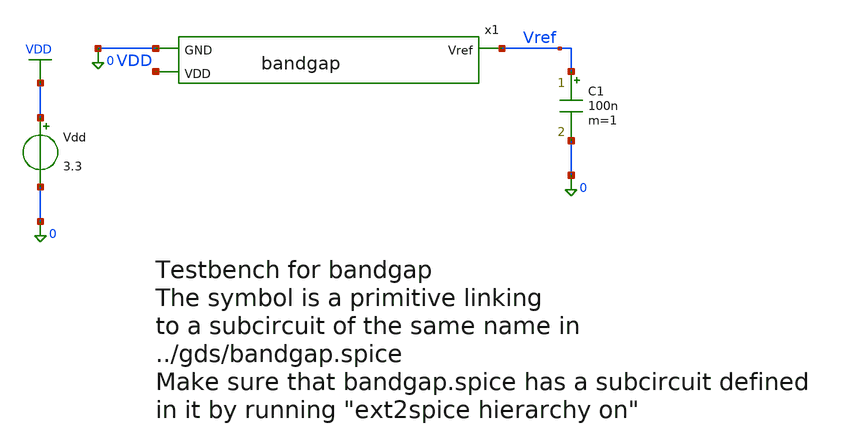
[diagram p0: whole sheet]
** sch_path: xschem/bandgap_tb.sch
* Copyright 2021 Stefan Frederik Schippers
* Licensed under the Apache License, Version 2.0 (the "License");
* you may not use this file except in compliance with the License.
* You may obtain a copy of the License at
* https://www.apache.org/licenses/LICENSE-2.0
* Unless required by applicable law or agreed to in writing, software
* distributed under the License is distributed on an "AS IS" BASIS,
* WITHOUT WARRANTIES OR CONDITIONS OF ANY KIND, either express or implied.
* See the License for the specific language governing permissions and
* limitations under the License.
**.subckt bandgap_tb
Vdd VDD 0 3.3
C1 Vref 0 100n m=1
x1 Vref VDD 0 bandgap
**** begin user architecture code

** opencircuitdesign pdks install
.lib $::SKYWATER_MODELS/sky130.lib.spice tt



.option wnflag=1
.include ../netlist/rcx/bandgap.spice
.save all
.control
set gnuplot_terminal=png/quit

op
#print x1.Vg1 x1.ve1 x1.vg10 x1.vg12 x1.vg2 x1.vg3 x1.vg5 x1.vs5
#tran 10n 10u
#plot V(Vref) title 'Vref vs time'

dc VDD 3.0 3.5 0.1
gnuplot bandgap_vref_vs_vdd V(Vref)  title 'Vref vs Vdd'  xlabel 'VDD' ylabel 'Vref'
#plot V(Vref) vs V(Vdd) title 'Vref vs Vdd'

dc VDD 3.0 3.5 0.02 TEMP -40 40 20
gnuplot bandgap_vref_vs_vdd_vs_temp V(Vref)  title 'Vref vs Vdd vs Temp (-40 to 40C)'  xlabel 'VDD' ylabel
+ 'Vref'
#plot V(Vref) Vs V(Vdd) title 'Vref vs Vdd vs Temp'

#dc TEMP -40 40 10
#plot V(Vref) title 'Vref vs Temp at VDD=3.3'

.endc


**** end user architecture code
**.ends

* expanding   symbol:  bandgap.sym # of pins=3
** sym_path: xschem/bandgap.sym
** sch_path: xschem/bandgap.sch
.subckt bandgap Vref VDD GND
*.opin Vref
*.ipin GND
*.ipin VDD
XM4 Vg3 Vg3 GND GND sky130_fd_pr__nfet_g5v0d10v5 L=1 W=20 nf=1 ad='int((1 + 1)/2) * 20 / 1 * 0.29' as='int((1 + 2)/2) * 20 / 1 * 0.29'
+ pd='2*int((1 + 1)/2) * (20 / 1 + 0.29)' ps='2*int((1 + 2)/2) * (20 / 1 + 0.29)' nrd='0.29 / 20 ' nrs='0.29 / 20 '
+ sa=0 sb=0 sd=0 mult=1 m=1
XQ1 GND GND Ve1 sky130_fd_pr__pnp_05v5_W3p40L3p40 m=24
XQ2 GND GND Vg2 sky130_fd_pr__pnp_05v5_W3p40L3p40 m=1
XM1 Vg10 Vg1 net1 net1 sky130_fd_pr__pfet_g5v0d10v5 L=1 W=20 nf=1 ad='int((1 + 1)/2) * 20 / 1 * 0.29'
+ as='int((1 + 2)/2) * 20 / 1 * 0.29' pd='2*int((1 + 1)/2) * (20 / 1 + 0.29)' ps='2*int((1 + 2)/2) * (20 / 1 + 0.29)'
+ nrd='0.29 / 20 ' nrs='0.29 / 20 ' sa=0 sb=0 sd=0 mult=1 m=1
XM2 Vg3 Vg2 net1 net1 sky130_fd_pr__pfet_g5v0d10v5 L=1 W=20 nf=1 ad='int((1 + 1)/2) * 20 / 1 * 0.29'
+ as='int((1 + 2)/2) * 20 / 1 * 0.29' pd='2*int((1 + 1)/2) * (20 / 1 + 0.29)' ps='2*int((1 + 2)/2) * (20 / 1 + 0.29)'
+ nrd='0.29 / 20 ' nrs='0.29 / 20 ' sa=0 sb=0 sd=0 mult=1 m=1
XM11 net1 Vg5 VDD VDD sky130_fd_pr__pfet_g5v0d10v5 L=1 W=1 nf=1 ad='int((1 + 1)/2) * 1 / 1 * 0.29' as='int((1 + 2)/2) * 1 / 1 * 0.29'
+ pd='2*int((1 + 1)/2) * (1 / 1 + 0.29)' ps='2*int((1 + 2)/2) * (1 / 1 + 0.29)' nrd='0.29 / 1 ' nrs='0.29 / 1 '
+ sa=0 sb=0 sd=0 mult=1 m=1
XM3 Vg10 Vg3 GND GND sky130_fd_pr__nfet_g5v0d10v5 L=1 W=20 nf=1 ad='int((1 + 1)/2) * 20 / 1 * 0.29' as='int((1 + 2)/2) * 20 / 1 * 0.29'
+ pd='2*int((1 + 1)/2) * (20 / 1 + 0.29)' ps='2*int((1 + 2)/2) * (20 / 1 + 0.29)' nrd='0.29 / 20 ' nrs='0.29 / 20 '
+ sa=0 sb=0 sd=0 mult=1 m=1
XM10 net2 Vg10 GND GND sky130_fd_pr__nfet_g5v0d10v5 L=1 W=20 nf=1 ad='int((1 + 1)/2) * 20 / 1 * 0.29'
+ as='int((1 + 2)/2) * 20 / 1 * 0.29' pd='2*int((1 + 1)/2) * (20 / 1 + 0.29)' ps='2*int((1 + 2)/2) * (20 / 1 + 0.29)'
+ nrd='0.29 / 20 ' nrs='0.29 / 20 ' sa=0 sb=0 sd=0 mult=1 m=1
XM8 Vg12 Vg5 VDD VDD sky130_fd_pr__pfet_g5v0d10v5 L=1 W=1 nf=1 ad='int((1 + 1)/2) * 1 / 1 * 0.29' as='int((1 + 2)/2) * 1 / 1 * 0.29'
+ pd='2*int((1 + 1)/2) * (1 / 1 + 0.29)' ps='2*int((1 + 2)/2) * (1 / 1 + 0.29)' nrd='0.29 / 1 ' nrs='0.29 / 1 '
+ sa=0 sb=0 sd=0 mult=1 m=1
XM5 Vg5 Vg5 VDD VDD sky130_fd_pr__pfet_g5v0d10v5 L=1 W=1 nf=1 ad='int((1 + 1)/2) * 1 / 1 * 0.29' as='int((1 + 2)/2) * 1 / 1 * 0.29'
+ pd='2*int((1 + 1)/2) * (1 / 1 + 0.29)' ps='2*int((1 + 2)/2) * (1 / 1 + 0.29)' nrd='0.29 / 1 ' nrs='0.29 / 1 '
+ sa=0 sb=0 sd=0 mult=1 m=1
XM12 Vref Vg12 VDD VDD sky130_fd_pr__pfet_g5v0d10v5 L=0.5 W=20 nf=1 ad='int((1 + 1)/2) * 20 / 1 * 0.29'
+ as='int((1 + 2)/2) * 20 / 1 * 0.29' pd='2*int((1 + 1)/2) * (20 / 1 + 0.29)' ps='2*int((1 + 2)/2) * (20 / 1 + 0.29)'
+ nrd='0.29 / 20 ' nrs='0.29 / 20 ' sa=0 sb=0 sd=0 mult=1 m=1
XM9 Vg12 Vref net2 GND sky130_fd_pr__nfet_g5v0d10v5 L=1 W=20 nf=1 ad='int((1 + 1)/2) * 20 / 1 * 0.29'
+ as='int((1 + 2)/2) * 20 / 1 * 0.29' pd='2*int((1 + 1)/2) * (20 / 1 + 0.29)' ps='2*int((1 + 2)/2) * (20 / 1 + 0.29)'
+ nrd='0.29 / 20 ' nrs='0.29 / 20 ' sa=0 sb=0 sd=0 mult=1 m=1
XM7a Vg12 Vg12 net6 GND sky130_fd_pr__nfet_g5v0d10v5 L=10 W=0.5 nf=1 ad='int((1 + 1)/2) * 0.5 / 1 * 0.29'
+ as='int((1 + 2)/2) * 0.5 / 1 * 0.29' pd='2*int((1 + 1)/2) * (0.5 / 1 + 0.29)' ps='2*int((1 + 2)/2) * (0.5 / 1 + 0.29)'
+ nrd='0.29 / 0.5 ' nrs='0.29 / 0.5 ' sa=0 sb=0 sd=0 mult=1 m=1
XM7b net6 Vg12 net5 GND sky130_fd_pr__nfet_g5v0d10v5 L=10 W=0.5 nf=1 ad='int((1 + 1)/2) * 0.5 / 1 * 0.29'
+ as='int((1 + 2)/2) * 0.5 / 1 * 0.29' pd='2*int((1 + 1)/2) * (0.5 / 1 + 0.29)' ps='2*int((1 + 2)/2) * (0.5 / 1 + 0.29)'
+ nrd='0.29 / 0.5 ' nrs='0.29 / 0.5 ' sa=0 sb=0 sd=0 mult=1 m=1
XM7c net5 Vg12 net4 GND sky130_fd_pr__nfet_g5v0d10v5 L=10 W=0.5 nf=1 ad='int((1 + 1)/2) * 0.5 / 1 * 0.29'
+ as='int((1 + 2)/2) * 0.5 / 1 * 0.29' pd='2*int((1 + 1)/2) * (0.5 / 1 + 0.29)' ps='2*int((1 + 2)/2) * (0.5 / 1 + 0.29)'
+ nrd='0.29 / 0.5 ' nrs='0.29 / 0.5 ' sa=0 sb=0 sd=0 mult=1 m=1
XM7d net4 Vg12 net3 GND sky130_fd_pr__nfet_g5v0d10v5 L=10 W=0.5 nf=1 ad='int((1 + 1)/2) * 0.5 / 1 * 0.29'
+ as='int((1 + 2)/2) * 0.5 / 1 * 0.29' pd='2*int((1 + 1)/2) * (0.5 / 1 + 0.29)' ps='2*int((1 + 2)/2) * (0.5 / 1 + 0.29)'
+ nrd='0.29 / 0.5 ' nrs='0.29 / 0.5 ' sa=0 sb=0 sd=0 mult=1 m=1
XM7e net3 Vg12 net11 GND sky130_fd_pr__nfet_g5v0d10v5 L=10 W=0.5 nf=1 ad='int((1 + 1)/2) * 0.5 / 1 * 0.29'
+ as='int((1 + 2)/2) * 0.5 / 1 * 0.29' pd='2*int((1 + 1)/2) * (0.5 / 1 + 0.29)' ps='2*int((1 + 2)/2) * (0.5 / 1 + 0.29)'
+ nrd='0.29 / 0.5 ' nrs='0.29 / 0.5 ' sa=0 sb=0 sd=0 mult=1 m=1
XM6 Vg5 Vref Vs5 GND sky130_fd_pr__nfet_g5v0d10v5 L=1 W=5 nf=1 ad='int((1 + 1)/2) * 5 / 1 * 0.29' as='int((1 + 2)/2) * 5 / 1 * 0.29'
+ pd='2*int((1 + 1)/2) * (5 / 1 + 0.29)' ps='2*int((1 + 2)/2) * (5 / 1 + 0.29)' nrd='0.29 / 5 ' nrs='0.29 / 5 '
+ sa=0 sb=0 sd=0 mult=1 m=1
XR1 Vg2 Vref GND sky130_fd_pr__res_high_po_0p35 L=20.1 mult=1 m=1
XR2 Vg1 Vref GND sky130_fd_pr__res_high_po_0p35 L=20.1 mult=1 m=1
XR4 GND Vs5 GND sky130_fd_pr__res_high_po_0p35 L=49.12 mult=1 m=1
XM7f net11 Vg12 net10 GND sky130_fd_pr__nfet_g5v0d10v5 L=10 W=0.5 nf=1 ad='int((1 + 1)/2) * 0.5 / 1 * 0.29'
+ as='int((1 + 2)/2) * 0.5 / 1 * 0.29' pd='2*int((1 + 1)/2) * (0.5 / 1 + 0.29)' ps='2*int((1 + 2)/2) * (0.5 / 1 + 0.29)'
+ nrd='0.29 / 0.5 ' nrs='0.29 / 0.5 ' sa=0 sb=0 sd=0 mult=1 m=1
XM7g net10 Vg12 net9 GND sky130_fd_pr__nfet_g5v0d10v5 L=10 W=0.5 nf=1 ad='int((1 + 1)/2) * 0.5 / 1 * 0.29'
+ as='int((1 + 2)/2) * 0.5 / 1 * 0.29' pd='2*int((1 + 1)/2) * (0.5 / 1 + 0.29)' ps='2*int((1 + 2)/2) * (0.5 / 1 + 0.29)'
+ nrd='0.29 / 0.5 ' nrs='0.29 / 0.5 ' sa=0 sb=0 sd=0 mult=1 m=1
XM7h net9 Vg12 net8 GND sky130_fd_pr__nfet_g5v0d10v5 L=10 W=0.5 nf=1 ad='int((1 + 1)/2) * 0.5 / 1 * 0.29'
+ as='int((1 + 2)/2) * 0.5 / 1 * 0.29' pd='2*int((1 + 1)/2) * (0.5 / 1 + 0.29)' ps='2*int((1 + 2)/2) * (0.5 / 1 + 0.29)'
+ nrd='0.29 / 0.5 ' nrs='0.29 / 0.5 ' sa=0 sb=0 sd=0 mult=1 m=1
XM7I net8 Vg12 net7 GND sky130_fd_pr__nfet_g5v0d10v5 L=10 W=0.5 nf=1 ad='int((1 + 1)/2) * 0.5 / 1 * 0.29'
+ as='int((1 + 2)/2) * 0.5 / 1 * 0.29' pd='2*int((1 + 1)/2) * (0.5 / 1 + 0.29)' ps='2*int((1 + 2)/2) * (0.5 / 1 + 0.29)'
+ nrd='0.29 / 0.5 ' nrs='0.29 / 0.5 ' sa=0 sb=0 sd=0 mult=1 m=1
XM7J net7 Vg12 GND GND sky130_fd_pr__nfet_g5v0d10v5 L=10 W=0.5 nf=1 ad='int((1 + 1)/2) * 0.5 / 1 * 0.29'
+ as='int((1 + 2)/2) * 0.5 / 1 * 0.29' pd='2*int((1 + 1)/2) * (0.5 / 1 + 0.29)' ps='2*int((1 + 2)/2) * (0.5 / 1 + 0.29)'
+ nrd='0.29 / 0.5 ' nrs='0.29 / 0.5 ' sa=0 sb=0 sd=0 mult=1 m=1
XR3 Ve1 Vg1 GND sky130_fd_pr__res_high_po_0p69 L=6.99 mult=1 m=1
.ends

.GLOBAL VDD
.GLOBAL GND
.end
